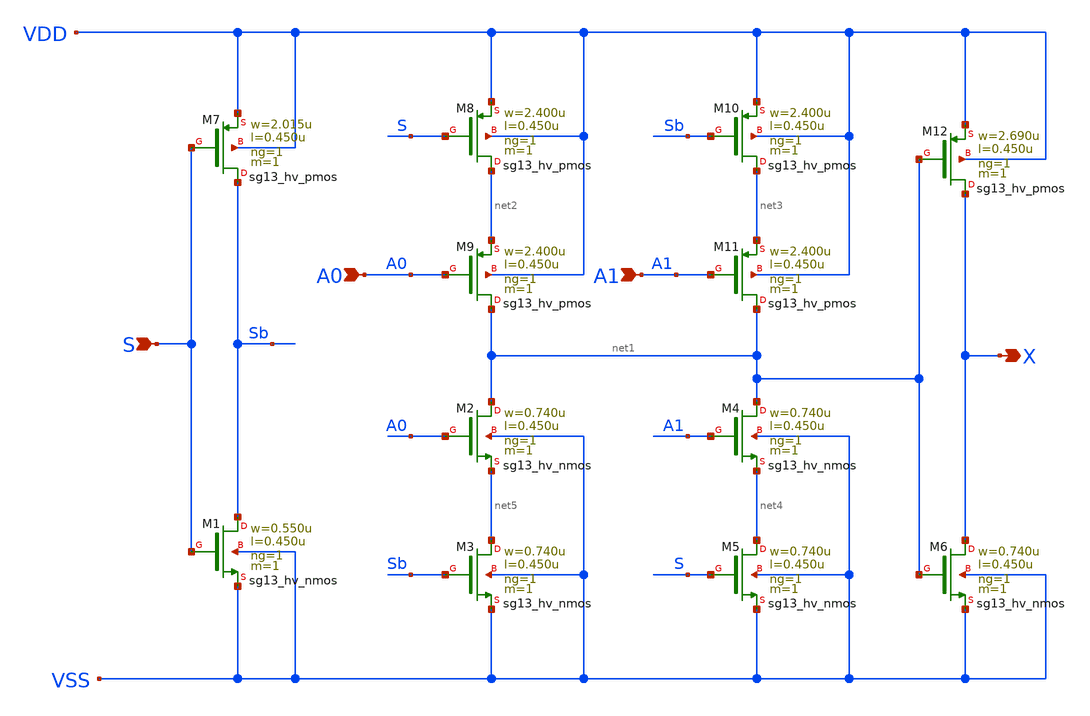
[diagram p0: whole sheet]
** sch_path: ihp-sg13g2/libs.ref/sg13g2_stdcell_hv/sch/xschem/sg13g2_hv_mux2_1.sch
* Copyright 2023 IHP PDK Authors
* Licensed under the Apache License, Version 2.0 (the "License");
* you may not use this file except in compliance with the License.
* You may obtain a copy of the License at
* https://www.apache.org/licenses/LICENSE-2.0
* Unless required by applicable law or agreed to in writing, software
* distributed under the License is distributed on an "AS IS" BASIS,
* WITHOUT WARRANTIES OR CONDITIONS OF ANY KIND, either express or implied.
* See the License for the specific language governing permissions and
* limitations under the License.
**.subckt sg13g2_hv_mux2_1 S A0 A1 X
*.ipin S
*.ipin A0
*.ipin A1
*.opin X
XM1 Sb S VSS VSS sg13_hv_nmos w=0.550u l=0.450u ng=1 m=1 mm_ok=1
XM2 net1 A0 net5 VSS sg13_hv_nmos w=0.740u l=0.450u ng=1 m=1 mm_ok=1
XM3 net5 Sb VSS VSS sg13_hv_nmos w=0.740u l=0.450u ng=1 m=1 mm_ok=1
XM4 net1 A1 net4 VSS sg13_hv_nmos w=0.740u l=0.450u ng=1 m=1 mm_ok=1
XM5 net4 S VSS VSS sg13_hv_nmos w=0.740u l=0.450u ng=1 m=1 mm_ok=1
XM6 X net1 VSS VSS sg13_hv_nmos w=0.740u l=0.450u ng=1 m=1 mm_ok=1
XM7 Sb S VDD VDD sg13_hv_pmos w=2.015u l=0.450u ng=1 m=1 mm_ok=1
XM8 net2 S VDD VDD sg13_hv_pmos w=2.400u l=0.450u ng=1 m=1 mm_ok=1
XM9 net1 A0 net2 VDD sg13_hv_pmos w=2.400u l=0.450u ng=1 m=1 mm_ok=1
XM10 net3 Sb VDD VDD sg13_hv_pmos w=2.400u l=0.450u ng=1 m=1 mm_ok=1
XM11 net1 A1 net3 VDD sg13_hv_pmos w=2.400u l=0.450u ng=1 m=1 mm_ok=1
XM12 X net1 VDD VDD sg13_hv_pmos w=2.690u l=0.450u ng=1 m=1 mm_ok=1
**.ends
.end
